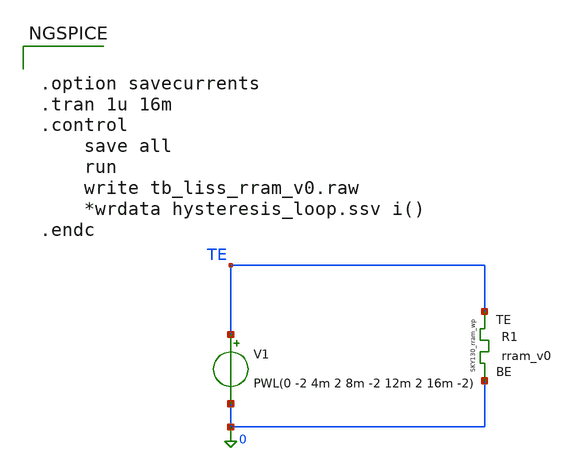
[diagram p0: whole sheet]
** sch_path: Ricardo/STDP_test/tb_liss_rram_v0.sch
**.subckt tb_liss_rram_v0
XR1 TE 0 rram_v0
V1 TE 0 PWL(0 -2 4m 2 8m -2 12m 2 16m -2)
**** begin user architecture code

** opencircuitdesign pdks install
.inc $::SKYWATER_MODELS/rram_v0.spice



.option savecurrents
.tran 1u 16m
.control
	save all
	run
	write tb_liss_rram_v0.raw
	*wrdata hysteresis_loop.ssv i()
.endc



**** end user architecture code
**.ends
.end
